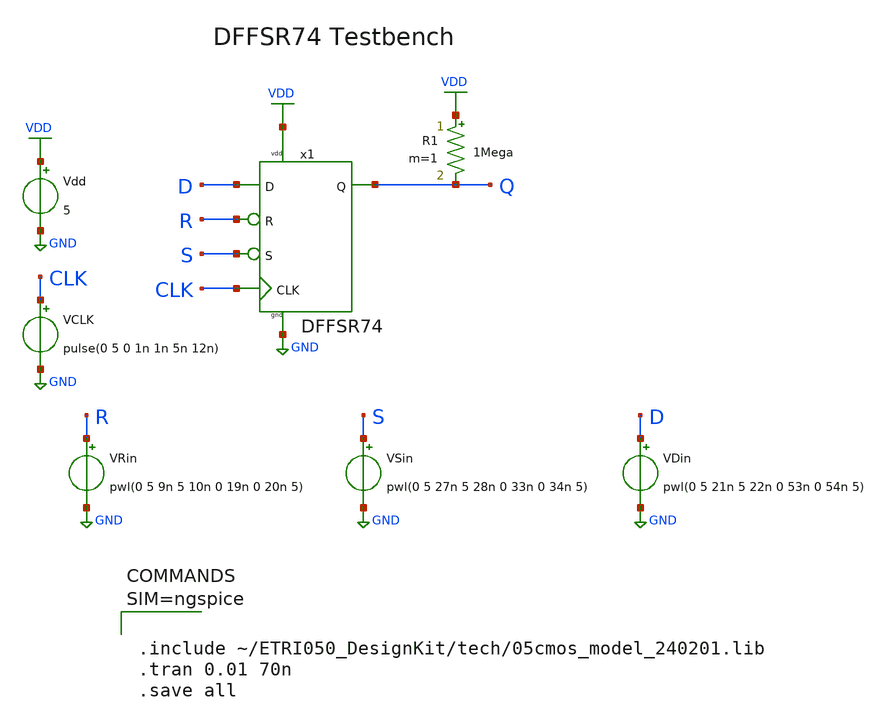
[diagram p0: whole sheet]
** sch_path: Tutorials/1-4_StdCell_DFFSR/Layout/DFFSR74_TB.sch
**.subckt DFFSR74_TB
Vdd VDD GND 5
VDin D GND pwl(0 5 21n 5 22n 0 53n 0 54n 5)
VRin R GND pwl(0 5 9n 5 10n 0 19n 0 20n 5)
VSin S GND pwl(0 5 27n 5 28n 0 33n 0 34n 5)
VCLK CLK GND pulse(0 5 0 1n 1n 5n 12n)
R1 VDD Q 1Mega m=1
x1 D R S CLK Q VDD GND DFFSR74
**** begin user architecture code



.include ~/ETRI050_DesignKit/tech/05cmos_model_240201.lib
.tran 0.01 70n
.save all



**** end user architecture code
**.ends

* expanding   symbol:
*+  /home/goodkook/ETRI050_DesignKit/Tutorials/1-4_StdCell_DFFSR/Layout/DFFSR74.sym # of pins=7
** sym_path: Tutorials/1-4_StdCell_DFFSR/Layout/DFFSR74.sym
.include ../DFFSR74.spice
.GLOBAL VDD
.GLOBAL GND
.end
